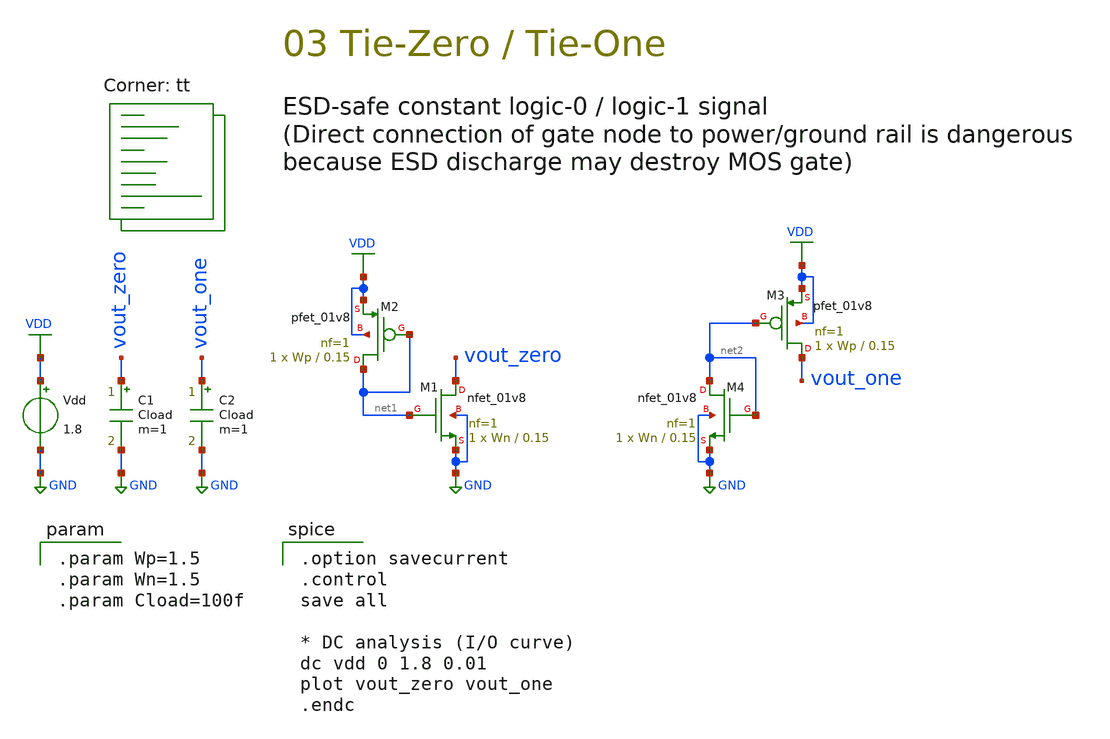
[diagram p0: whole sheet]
** sch_path: 03-a_tie.sch
**.subckt 03-a_tie
Vdd VDD GND 1.8
XM2 net1 net1 VDD VDD sky130_fd_pr__pfet_01v8 L=0.15 W=Wp nf=1 ad='int((nf+1)/2) * W/nf * 0.29' as='int((nf+2)/2) * W/nf * 0.29'
+ pd='2*int((nf+1)/2) * (W/nf + 0.29)' ps='2*int((nf+2)/2) * (W/nf + 0.29)' nrd='0.29 / W' nrs='0.29 / W'
+ sa=0 sb=0 sd=0 mult=1 m=1
XM1 vout_zero net1 GND GND sky130_fd_pr__nfet_01v8 L=0.15 W=Wn nf=1 ad='int((1 + 1)/2) * Wn / 1 * 0.29'
+ as='int((1 + 2)/2) * Wn / 1 * 0.29' pd='2*int((1 + 1)/2) * (Wn / 1 + 0.29)' ps='2*int((1 + 2)/2) * (Wn / 1 + 0.29)'
+ nrd='0.29 / Wn ' nrs='0.29 / Wn ' sa=0 sb=0 sd=0 mult=1 m=1
XM3 vout_one net2 VDD VDD sky130_fd_pr__pfet_01v8 L=0.15 W=Wp nf=1 ad='int((nf+1)/2) * W/nf * 0.29' as='int((nf+2)/2) * W/nf * 0.29'
+ pd='2*int((nf+1)/2) * (W/nf + 0.29)' ps='2*int((nf+2)/2) * (W/nf + 0.29)' nrd='0.29 / W' nrs='0.29 / W'
+ sa=0 sb=0 sd=0 mult=1 m=1
XM4 net2 net2 GND GND sky130_fd_pr__nfet_01v8 L=0.15 W=Wn nf=1 ad='int((1 + 1)/2) * Wn / 1 * 0.29' as='int((1 + 2)/2) * Wn / 1 * 0.29'
+ pd='2*int((1 + 1)/2) * (Wn / 1 + 0.29)' ps='2*int((1 + 2)/2) * (Wn / 1 + 0.29)' nrd='0.29 / Wn ' nrs='0.29 / Wn '
+ sa=0 sb=0 sd=0 mult=1 m=1
C2 vout_one GND Cload m=1
C1 vout_zero GND Cload m=1
**** begin user architecture code
.lib $::SKYWATER_MODELS/sky130.lib.spice tt

.param Wp=1.5
.param Wn=1.5
.param Cload=100f


.option savecurrent
.control
save all

* DC analysis (I/O curve)
dc vdd 0 1.8 0.01
plot vout_zero vout_one
.endc

**** end user architecture code
**.ends
.GLOBAL GND
.GLOBAL VDD
.end
